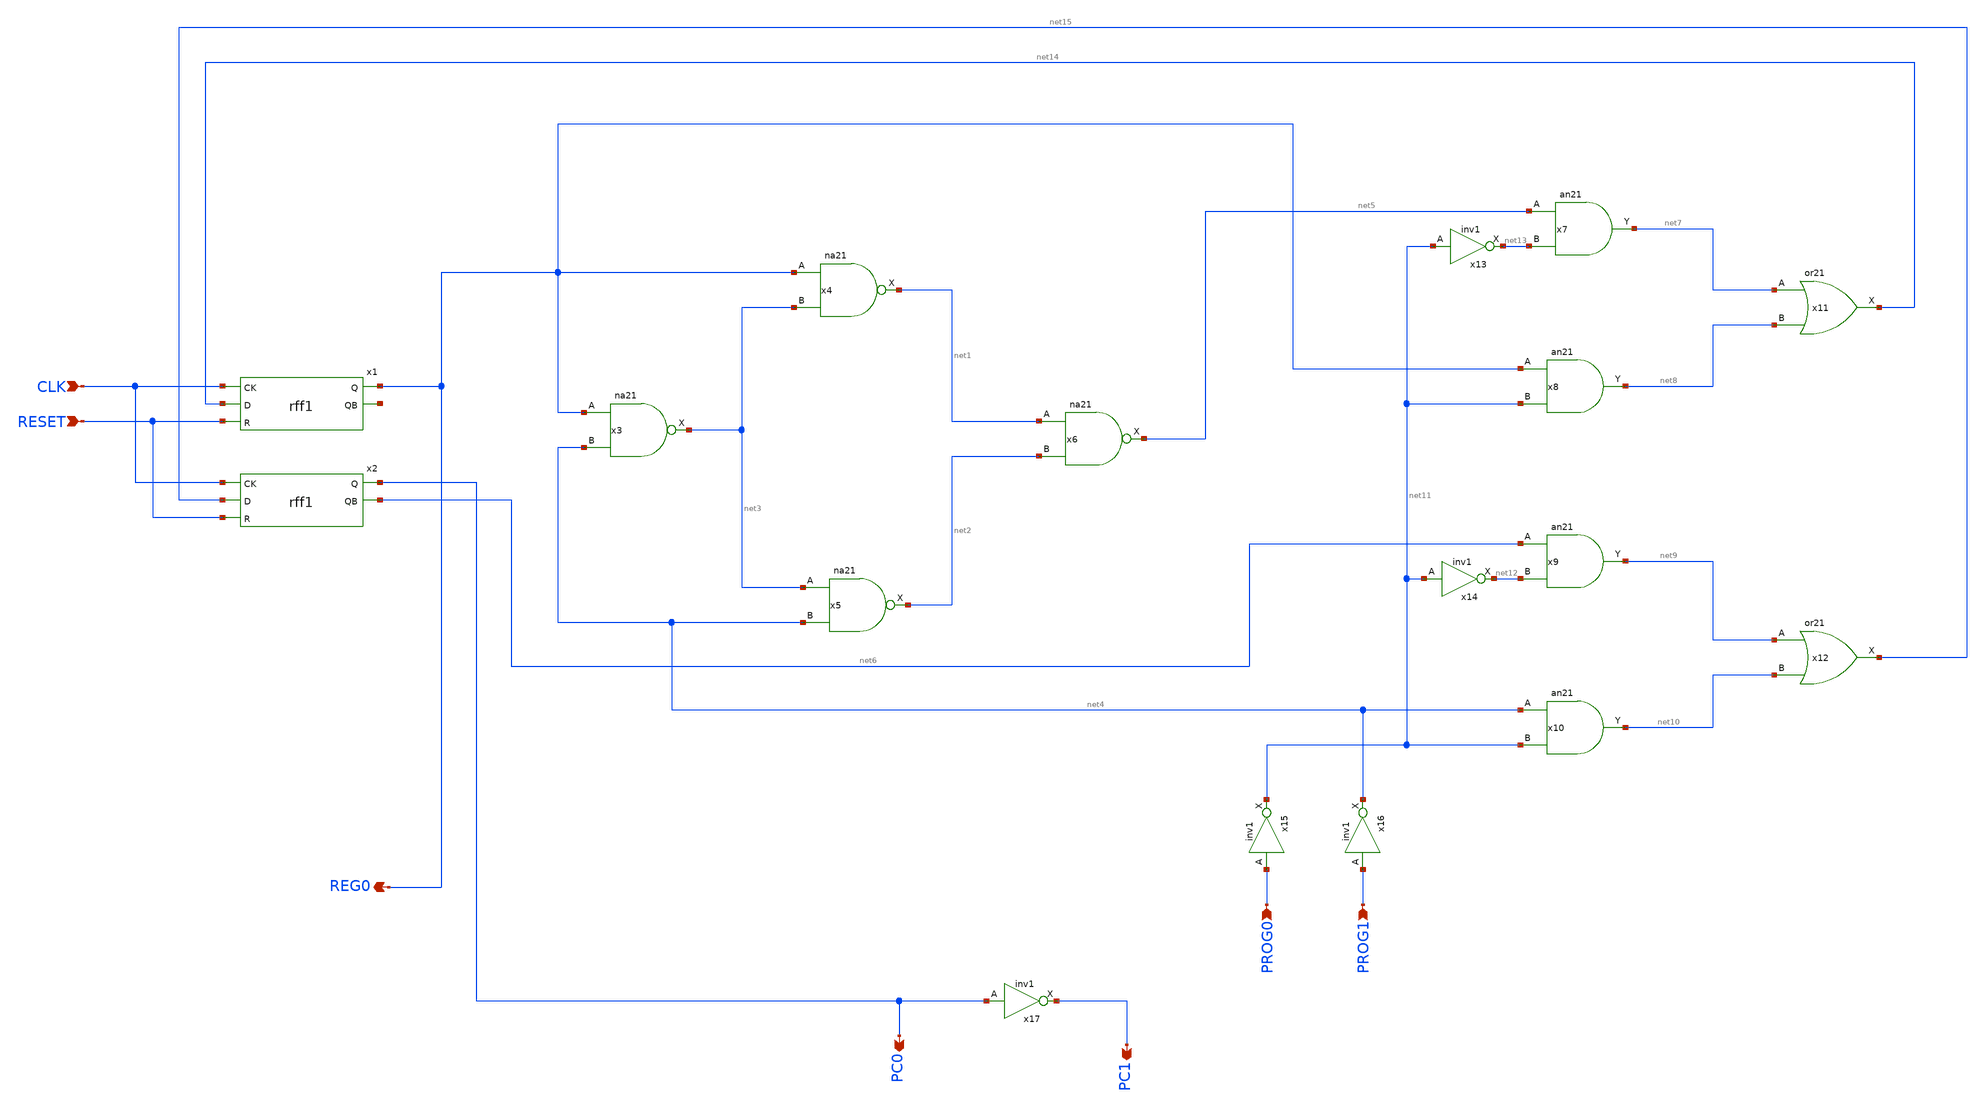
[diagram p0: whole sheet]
** sch_path: member_project/GxP/xschem/1bit-CPU.sch
**.subckt 1bit-CPU CLK RESET PROG1 PROG0 REG0 PC0 PC1
*.ipin CLK
*.ipin RESET
*.ipin PROG1
*.ipin PROG0
*.opin REG0
*.opin PC0
*.opin PC1
x3 REG0 net4 VDD GND net3 na21
x4 REG0 net3 VDD GND net1 na21
x5 net3 net4 VDD GND net2 na21
x6 net1 net2 VDD GND net5 na21
x7 net5 net13 VDD GND net7 an21
x8 REG0 net11 VDD GND net8 an21
x9 net6 net12 VDD GND net9 an21
x10 net4 net11 VDD GND net10 an21
x13 net11 VDD GND net13 inv1
x14 net11 VDD GND net12 inv1
x15 PROG0 VDD GND net11 inv1
x16 PROG1 VDD GND net4 inv1
x17 PC0 VDD GND PC1 inv1
x11 net7 net8 VDD GND net14 or21
x12 net9 net10 VDD GND net15 or21
x1 CLK net14 REG0 net16 RESET VDD GND rff1
x2 CLK net15 PC0 net6 RESET VDD GND rff1
**.ends
.end
